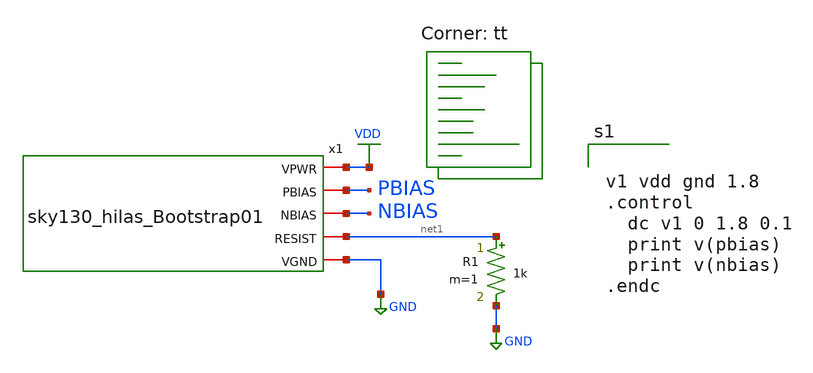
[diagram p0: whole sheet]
** sch_path: project2/bootstrap_demo.sch
**.subckt bootstrap_demo
x1 VDD PBIAS NBIAS net1 GND sky130_hilas_Bootstrap01
R1 net1 GND 1k m=1
**** begin user architecture code


v1 vdd gnd 1.8
.control
  dc v1 0 1.8 0.1
  print v(pbias)
  print v(nbias)
.endc




.lib $::SKYWATER_MODELS/sky130.lib.spice tt
**** end user architecture code
**.ends

* expanding   symbol:  sky130_hilas_Bootstrap01.sym # of pins=5
** sym_path: project2/sky130_hilas_Bootstrap01.sym
** sch_path: project2/sky130_hilas_Bootstrap01.sch
.subckt sky130_hilas_Bootstrap01 VPWR PBIAS NBIAS RESIST VGND
*.iopin VPWR
*.iopin NBIAS
*.iopin PBIAS
*.iopin VGND
*.iopin RESIST
*.iopin RESIST
*.iopin VPWR
*.iopin VGND
XM4 NBIAS NBIAS VGND VGND sky130_fd_pr__nfet_01v8 L=0.2 W=2 nf=1 ad='int((nf+1)/2) * W/nf * 0.29' as='int((nf+2)/2) * W/nf * 0.29'
+ pd='2*int((nf+1)/2) * (W/nf + 0.29)' ps='2*int((nf+2)/2) * (W/nf + 0.29)' nrd='0.29 / W' nrs='0.29 / W'
+ sa=0 sb=0 sd=0 mult=1 m=1
XM7 NBIAS PBIAS VPWR VPWR sky130_fd_pr__pfet_01v8 L=0.2 W=5.81 nf=1 ad='int((nf+1)/2) * W/nf * 0.29'
+ as='int((nf+2)/2) * W/nf * 0.29' pd='2*int((nf+1)/2) * (W/nf + 0.29)' ps='2*int((nf+2)/2) * (W/nf + 0.29)'
+ nrd='0.29 / W' nrs='0.29 / W' sa=0 sb=0 sd=0 mult=1 m=1
XM10 PBIAS NBIAS net1 VGND sky130_fd_pr__nfet_01v8 L=0.2 W=95.36 nf=1 ad='int((nf+1)/2) * W/nf * 0.29'
+ as='int((nf+2)/2) * W/nf * 0.29' pd='2*int((nf+1)/2) * (W/nf + 0.29)' ps='2*int((nf+2)/2) * (W/nf + 0.29)'
+ nrd='0.29 / W' nrs='0.29 / W' sa=0 sb=0 sd=0 mult=1 m=1
XM5 PBIAS PBIAS VPWR VPWR sky130_fd_pr__pfet_01v8 L=0.2 W=5.81 nf=1 ad='int((nf+1)/2) * W/nf * 0.29'
+ as='int((nf+2)/2) * W/nf * 0.29' pd='2*int((nf+1)/2) * (W/nf + 0.29)' ps='2*int((nf+2)/2) * (W/nf + 0.29)'
+ nrd='0.29 / W' nrs='0.29 / W' sa=0 sb=0 sd=0 mult=1 m=1
XR1 RESIST net1 sky130_fd_pr__res_generic_po W=0.42 L=10.14 m=1
V1 net2 VGND 0
**** begin user architecture code


.control
  dc v2 0 1.8 0.1
  print i(v1)
  print v(NBIAS)
  print v(PBIAS)
.endc


**** end user architecture code
**** begin user architecture code
.lib $::SKYWATER_MODELS/sky130.lib.spice tt
**** end user architecture code
V2 VPWR VGND 1.8
V3 VGND GND 0
R2 RESIST net2 100k m=1
.ends

.GLOBAL GND
.GLOBAL VDD
.GLOBAL VGND
.end
